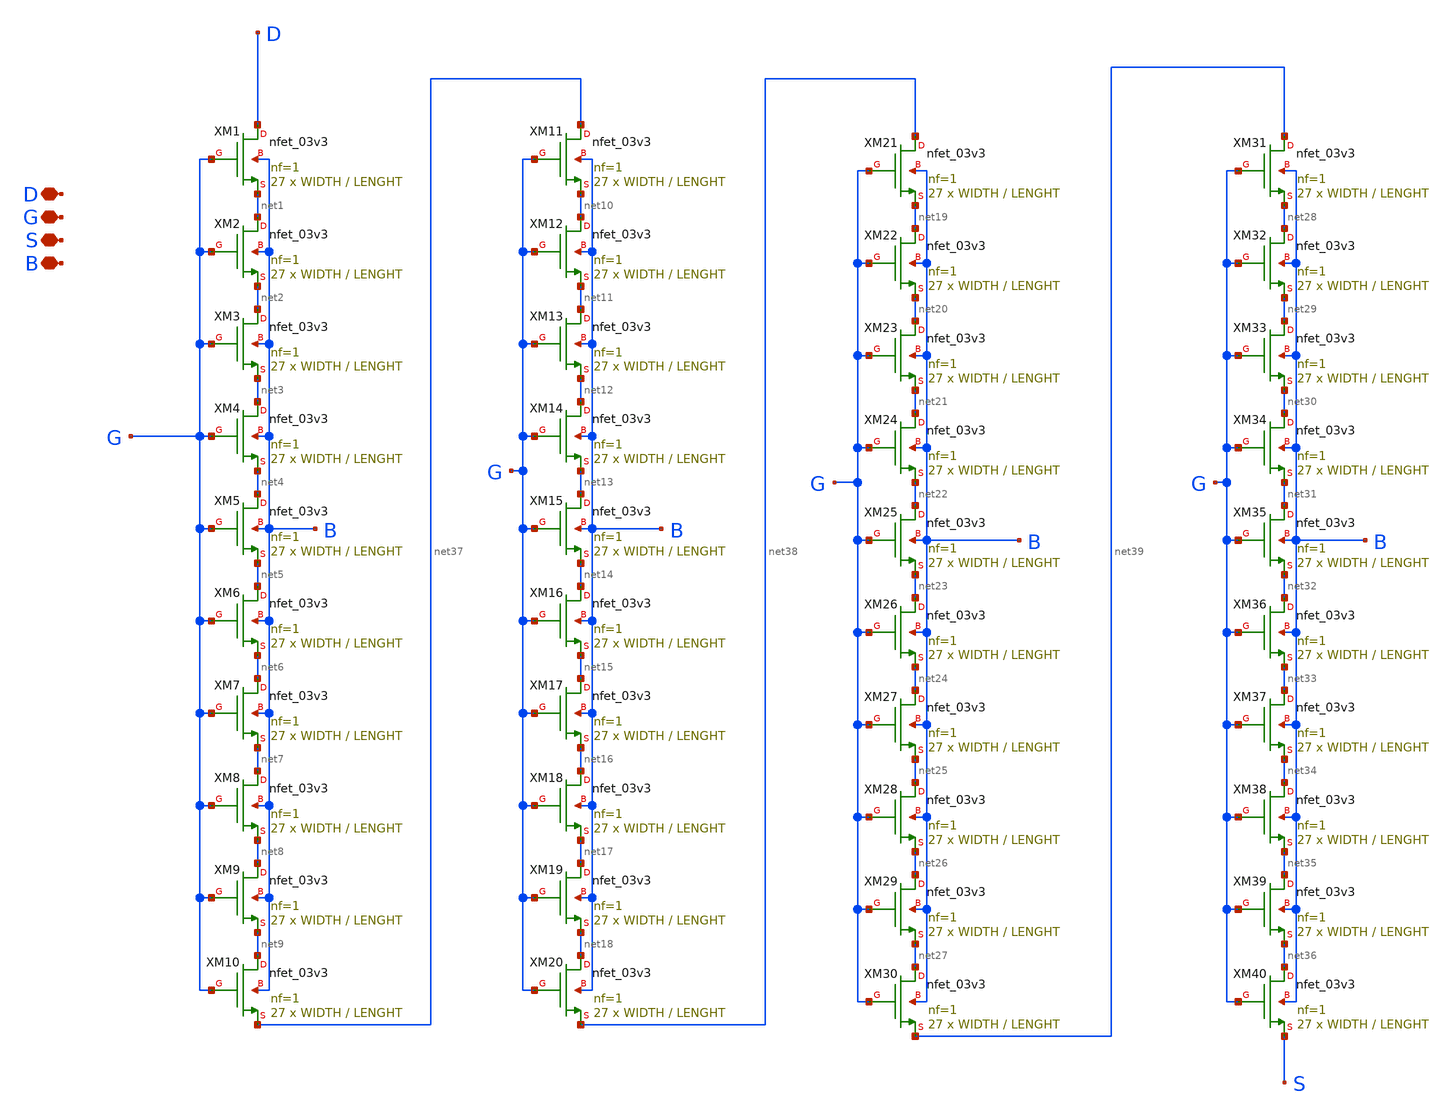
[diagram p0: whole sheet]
** sch_path: New_Extraction/Association/M5_ass.sch
**.subckt M5_ass D G S B
*.iopin D
*.iopin G
*.iopin S
*.iopin B
XM1 D G net1 B nfet_03v3 L=LENGHT W=WIDTH nf=1 ad='int((nf+1)/2) * W/nf * 0.18u' as='int((nf+2)/2) * W/nf * 0.18u'
+ pd='2*int((nf+1)/2) * (W/nf + 0.18u)' ps='2*int((nf+2)/2) * (W/nf + 0.18u)' nrd='0.18u / W' nrs='0.18u / W'
+ sa=0 sb=0 sd=0 m=27
XM2 net1 G net2 B nfet_03v3 L=LENGHT W=WIDTH nf=1 ad='int((nf+1)/2) * W/nf * 0.18u' as='int((nf+2)/2) * W/nf * 0.18u'
+ pd='2*int((nf+1)/2) * (W/nf + 0.18u)' ps='2*int((nf+2)/2) * (W/nf + 0.18u)' nrd='0.18u / W' nrs='0.18u / W'
+ sa=0 sb=0 sd=0 m=27
XM3 net2 G net3 B nfet_03v3 L=LENGHT W=WIDTH nf=1 ad='int((nf+1)/2) * W/nf * 0.18u' as='int((nf+2)/2) * W/nf * 0.18u'
+ pd='2*int((nf+1)/2) * (W/nf + 0.18u)' ps='2*int((nf+2)/2) * (W/nf + 0.18u)' nrd='0.18u / W' nrs='0.18u / W'
+ sa=0 sb=0 sd=0 m=27
XM4 net3 G net4 B nfet_03v3 L=LENGHT W=WIDTH nf=1 ad='int((nf+1)/2) * W/nf * 0.18u' as='int((nf+2)/2) * W/nf * 0.18u'
+ pd='2*int((nf+1)/2) * (W/nf + 0.18u)' ps='2*int((nf+2)/2) * (W/nf + 0.18u)' nrd='0.18u / W' nrs='0.18u / W'
+ sa=0 sb=0 sd=0 m=27
XM5 net4 G net5 B nfet_03v3 L=LENGHT W=WIDTH nf=1 ad='int((nf+1)/2) * W/nf * 0.18u' as='int((nf+2)/2) * W/nf * 0.18u'
+ pd='2*int((nf+1)/2) * (W/nf + 0.18u)' ps='2*int((nf+2)/2) * (W/nf + 0.18u)' nrd='0.18u / W' nrs='0.18u / W'
+ sa=0 sb=0 sd=0 m=27
XM6 net5 G net6 B nfet_03v3 L=LENGHT W=WIDTH nf=1 ad='int((nf+1)/2) * W/nf * 0.18u' as='int((nf+2)/2) * W/nf * 0.18u'
+ pd='2*int((nf+1)/2) * (W/nf + 0.18u)' ps='2*int((nf+2)/2) * (W/nf + 0.18u)' nrd='0.18u / W' nrs='0.18u / W'
+ sa=0 sb=0 sd=0 m=27
XM7 net6 G net7 B nfet_03v3 L=LENGHT W=WIDTH nf=1 ad='int((nf+1)/2) * W/nf * 0.18u' as='int((nf+2)/2) * W/nf * 0.18u'
+ pd='2*int((nf+1)/2) * (W/nf + 0.18u)' ps='2*int((nf+2)/2) * (W/nf + 0.18u)' nrd='0.18u / W' nrs='0.18u / W'
+ sa=0 sb=0 sd=0 m=27
XM8 net7 G net8 B nfet_03v3 L=LENGHT W=WIDTH nf=1 ad='int((nf+1)/2) * W/nf * 0.18u' as='int((nf+2)/2) * W/nf * 0.18u'
+ pd='2*int((nf+1)/2) * (W/nf + 0.18u)' ps='2*int((nf+2)/2) * (W/nf + 0.18u)' nrd='0.18u / W' nrs='0.18u / W'
+ sa=0 sb=0 sd=0 m=27
XM9 net8 G net9 B nfet_03v3 L=LENGHT W=WIDTH nf=1 ad='int((nf+1)/2) * W/nf * 0.18u' as='int((nf+2)/2) * W/nf * 0.18u'
+ pd='2*int((nf+1)/2) * (W/nf + 0.18u)' ps='2*int((nf+2)/2) * (W/nf + 0.18u)' nrd='0.18u / W' nrs='0.18u / W'
+ sa=0 sb=0 sd=0 m=27
XM10 net9 G net37 B nfet_03v3 L=LENGHT W=WIDTH nf=1 ad='int((nf+1)/2) * W/nf * 0.18u' as='int((nf+2)/2) * W/nf * 0.18u'
+ pd='2*int((nf+1)/2) * (W/nf + 0.18u)' ps='2*int((nf+2)/2) * (W/nf + 0.18u)' nrd='0.18u / W' nrs='0.18u / W'
+ sa=0 sb=0 sd=0 m=27
XM11 net37 G net10 B nfet_03v3 L=LENGHT W=WIDTH nf=1 ad='int((nf+1)/2) * W/nf * 0.18u' as='int((nf+2)/2) * W/nf * 0.18u'
+ pd='2*int((nf+1)/2) * (W/nf + 0.18u)' ps='2*int((nf+2)/2) * (W/nf + 0.18u)' nrd='0.18u / W' nrs='0.18u / W'
+ sa=0 sb=0 sd=0 m=27
XM12 net10 G net11 B nfet_03v3 L=LENGHT W=WIDTH nf=1 ad='int((nf+1)/2) * W/nf * 0.18u' as='int((nf+2)/2) * W/nf * 0.18u'
+ pd='2*int((nf+1)/2) * (W/nf + 0.18u)' ps='2*int((nf+2)/2) * (W/nf + 0.18u)' nrd='0.18u / W' nrs='0.18u / W'
+ sa=0 sb=0 sd=0 m=27
XM13 net11 G net12 B nfet_03v3 L=LENGHT W=WIDTH nf=1 ad='int((nf+1)/2) * W/nf * 0.18u' as='int((nf+2)/2) * W/nf * 0.18u'
+ pd='2*int((nf+1)/2) * (W/nf + 0.18u)' ps='2*int((nf+2)/2) * (W/nf + 0.18u)' nrd='0.18u / W' nrs='0.18u / W'
+ sa=0 sb=0 sd=0 m=27
XM14 net12 G net13 B nfet_03v3 L=LENGHT W=WIDTH nf=1 ad='int((nf+1)/2) * W/nf * 0.18u' as='int((nf+2)/2) * W/nf * 0.18u'
+ pd='2*int((nf+1)/2) * (W/nf + 0.18u)' ps='2*int((nf+2)/2) * (W/nf + 0.18u)' nrd='0.18u / W' nrs='0.18u / W'
+ sa=0 sb=0 sd=0 m=27
XM15 net13 G net14 B nfet_03v3 L=LENGHT W=WIDTH nf=1 ad='int((nf+1)/2) * W/nf * 0.18u' as='int((nf+2)/2) * W/nf * 0.18u'
+ pd='2*int((nf+1)/2) * (W/nf + 0.18u)' ps='2*int((nf+2)/2) * (W/nf + 0.18u)' nrd='0.18u / W' nrs='0.18u / W'
+ sa=0 sb=0 sd=0 m=27
XM16 net14 G net15 B nfet_03v3 L=LENGHT W=WIDTH nf=1 ad='int((nf+1)/2) * W/nf * 0.18u' as='int((nf+2)/2) * W/nf * 0.18u'
+ pd='2*int((nf+1)/2) * (W/nf + 0.18u)' ps='2*int((nf+2)/2) * (W/nf + 0.18u)' nrd='0.18u / W' nrs='0.18u / W'
+ sa=0 sb=0 sd=0 m=27
XM17 net15 G net16 B nfet_03v3 L=LENGHT W=WIDTH nf=1 ad='int((nf+1)/2) * W/nf * 0.18u' as='int((nf+2)/2) * W/nf * 0.18u'
+ pd='2*int((nf+1)/2) * (W/nf + 0.18u)' ps='2*int((nf+2)/2) * (W/nf + 0.18u)' nrd='0.18u / W' nrs='0.18u / W'
+ sa=0 sb=0 sd=0 m=27
XM18 net16 G net17 B nfet_03v3 L=LENGHT W=WIDTH nf=1 ad='int((nf+1)/2) * W/nf * 0.18u' as='int((nf+2)/2) * W/nf * 0.18u'
+ pd='2*int((nf+1)/2) * (W/nf + 0.18u)' ps='2*int((nf+2)/2) * (W/nf + 0.18u)' nrd='0.18u / W' nrs='0.18u / W'
+ sa=0 sb=0 sd=0 m=27
XM19 net17 G net18 B nfet_03v3 L=LENGHT W=WIDTH nf=1 ad='int((nf+1)/2) * W/nf * 0.18u' as='int((nf+2)/2) * W/nf * 0.18u'
+ pd='2*int((nf+1)/2) * (W/nf + 0.18u)' ps='2*int((nf+2)/2) * (W/nf + 0.18u)' nrd='0.18u / W' nrs='0.18u / W'
+ sa=0 sb=0 sd=0 m=27
XM20 net18 G net38 B nfet_03v3 L=LENGHT W=WIDTH nf=1 ad='int((nf+1)/2) * W/nf * 0.18u' as='int((nf+2)/2) * W/nf * 0.18u'
+ pd='2*int((nf+1)/2) * (W/nf + 0.18u)' ps='2*int((nf+2)/2) * (W/nf + 0.18u)' nrd='0.18u / W' nrs='0.18u / W'
+ sa=0 sb=0 sd=0 m=27
XM21 net38 G net19 B nfet_03v3 L=LENGHT W=WIDTH nf=1 ad='int((nf+1)/2) * W/nf * 0.18u' as='int((nf+2)/2) * W/nf * 0.18u'
+ pd='2*int((nf+1)/2) * (W/nf + 0.18u)' ps='2*int((nf+2)/2) * (W/nf + 0.18u)' nrd='0.18u / W' nrs='0.18u / W'
+ sa=0 sb=0 sd=0 m=27
XM22 net19 G net20 B nfet_03v3 L=LENGHT W=WIDTH nf=1 ad='int((nf+1)/2) * W/nf * 0.18u' as='int((nf+2)/2) * W/nf * 0.18u'
+ pd='2*int((nf+1)/2) * (W/nf + 0.18u)' ps='2*int((nf+2)/2) * (W/nf + 0.18u)' nrd='0.18u / W' nrs='0.18u / W'
+ sa=0 sb=0 sd=0 m=27
XM23 net20 G net21 B nfet_03v3 L=LENGHT W=WIDTH nf=1 ad='int((nf+1)/2) * W/nf * 0.18u' as='int((nf+2)/2) * W/nf * 0.18u'
+ pd='2*int((nf+1)/2) * (W/nf + 0.18u)' ps='2*int((nf+2)/2) * (W/nf + 0.18u)' nrd='0.18u / W' nrs='0.18u / W'
+ sa=0 sb=0 sd=0 m=27
XM24 net21 G net22 B nfet_03v3 L=LENGHT W=WIDTH nf=1 ad='int((nf+1)/2) * W/nf * 0.18u' as='int((nf+2)/2) * W/nf * 0.18u'
+ pd='2*int((nf+1)/2) * (W/nf + 0.18u)' ps='2*int((nf+2)/2) * (W/nf + 0.18u)' nrd='0.18u / W' nrs='0.18u / W'
+ sa=0 sb=0 sd=0 m=27
XM25 net22 G net23 B nfet_03v3 L=LENGHT W=WIDTH nf=1 ad='int((nf+1)/2) * W/nf * 0.18u' as='int((nf+2)/2) * W/nf * 0.18u'
+ pd='2*int((nf+1)/2) * (W/nf + 0.18u)' ps='2*int((nf+2)/2) * (W/nf + 0.18u)' nrd='0.18u / W' nrs='0.18u / W'
+ sa=0 sb=0 sd=0 m=27
XM26 net23 G net24 B nfet_03v3 L=LENGHT W=WIDTH nf=1 ad='int((nf+1)/2) * W/nf * 0.18u' as='int((nf+2)/2) * W/nf * 0.18u'
+ pd='2*int((nf+1)/2) * (W/nf + 0.18u)' ps='2*int((nf+2)/2) * (W/nf + 0.18u)' nrd='0.18u / W' nrs='0.18u / W'
+ sa=0 sb=0 sd=0 m=27
XM27 net24 G net25 B nfet_03v3 L=LENGHT W=WIDTH nf=1 ad='int((nf+1)/2) * W/nf * 0.18u' as='int((nf+2)/2) * W/nf * 0.18u'
+ pd='2*int((nf+1)/2) * (W/nf + 0.18u)' ps='2*int((nf+2)/2) * (W/nf + 0.18u)' nrd='0.18u / W' nrs='0.18u / W'
+ sa=0 sb=0 sd=0 m=27
XM28 net25 G net26 B nfet_03v3 L=LENGHT W=WIDTH nf=1 ad='int((nf+1)/2) * W/nf * 0.18u' as='int((nf+2)/2) * W/nf * 0.18u'
+ pd='2*int((nf+1)/2) * (W/nf + 0.18u)' ps='2*int((nf+2)/2) * (W/nf + 0.18u)' nrd='0.18u / W' nrs='0.18u / W'
+ sa=0 sb=0 sd=0 m=27
XM29 net26 G net27 B nfet_03v3 L=LENGHT W=WIDTH nf=1 ad='int((nf+1)/2) * W/nf * 0.18u' as='int((nf+2)/2) * W/nf * 0.18u'
+ pd='2*int((nf+1)/2) * (W/nf + 0.18u)' ps='2*int((nf+2)/2) * (W/nf + 0.18u)' nrd='0.18u / W' nrs='0.18u / W'
+ sa=0 sb=0 sd=0 m=27
XM30 net27 G net39 B nfet_03v3 L=LENGHT W=WIDTH nf=1 ad='int((nf+1)/2) * W/nf * 0.18u' as='int((nf+2)/2) * W/nf * 0.18u'
+ pd='2*int((nf+1)/2) * (W/nf + 0.18u)' ps='2*int((nf+2)/2) * (W/nf + 0.18u)' nrd='0.18u / W' nrs='0.18u / W'
+ sa=0 sb=0 sd=0 m=27
XM31 net39 G net28 B nfet_03v3 L=LENGHT W=WIDTH nf=1 ad='int((nf+1)/2) * W/nf * 0.18u' as='int((nf+2)/2) * W/nf * 0.18u'
+ pd='2*int((nf+1)/2) * (W/nf + 0.18u)' ps='2*int((nf+2)/2) * (W/nf + 0.18u)' nrd='0.18u / W' nrs='0.18u / W'
+ sa=0 sb=0 sd=0 m=27
XM32 net28 G net29 B nfet_03v3 L=LENGHT W=WIDTH nf=1 ad='int((nf+1)/2) * W/nf * 0.18u' as='int((nf+2)/2) * W/nf * 0.18u'
+ pd='2*int((nf+1)/2) * (W/nf + 0.18u)' ps='2*int((nf+2)/2) * (W/nf + 0.18u)' nrd='0.18u / W' nrs='0.18u / W'
+ sa=0 sb=0 sd=0 m=27
XM33 net29 G net30 B nfet_03v3 L=LENGHT W=WIDTH nf=1 ad='int((nf+1)/2) * W/nf * 0.18u' as='int((nf+2)/2) * W/nf * 0.18u'
+ pd='2*int((nf+1)/2) * (W/nf + 0.18u)' ps='2*int((nf+2)/2) * (W/nf + 0.18u)' nrd='0.18u / W' nrs='0.18u / W'
+ sa=0 sb=0 sd=0 m=27
XM34 net30 G net31 B nfet_03v3 L=LENGHT W=WIDTH nf=1 ad='int((nf+1)/2) * W/nf * 0.18u' as='int((nf+2)/2) * W/nf * 0.18u'
+ pd='2*int((nf+1)/2) * (W/nf + 0.18u)' ps='2*int((nf+2)/2) * (W/nf + 0.18u)' nrd='0.18u / W' nrs='0.18u / W'
+ sa=0 sb=0 sd=0 m=27
XM35 net31 G net32 B nfet_03v3 L=LENGHT W=WIDTH nf=1 ad='int((nf+1)/2) * W/nf * 0.18u' as='int((nf+2)/2) * W/nf * 0.18u'
+ pd='2*int((nf+1)/2) * (W/nf + 0.18u)' ps='2*int((nf+2)/2) * (W/nf + 0.18u)' nrd='0.18u / W' nrs='0.18u / W'
+ sa=0 sb=0 sd=0 m=27
XM36 net32 G net33 B nfet_03v3 L=LENGHT W=WIDTH nf=1 ad='int((nf+1)/2) * W/nf * 0.18u' as='int((nf+2)/2) * W/nf * 0.18u'
+ pd='2*int((nf+1)/2) * (W/nf + 0.18u)' ps='2*int((nf+2)/2) * (W/nf + 0.18u)' nrd='0.18u / W' nrs='0.18u / W'
+ sa=0 sb=0 sd=0 m=27
XM37 net33 G net34 B nfet_03v3 L=LENGHT W=WIDTH nf=1 ad='int((nf+1)/2) * W/nf * 0.18u' as='int((nf+2)/2) * W/nf * 0.18u'
+ pd='2*int((nf+1)/2) * (W/nf + 0.18u)' ps='2*int((nf+2)/2) * (W/nf + 0.18u)' nrd='0.18u / W' nrs='0.18u / W'
+ sa=0 sb=0 sd=0 m=27
XM38 net34 G net35 B nfet_03v3 L=LENGHT W=WIDTH nf=1 ad='int((nf+1)/2) * W/nf * 0.18u' as='int((nf+2)/2) * W/nf * 0.18u'
+ pd='2*int((nf+1)/2) * (W/nf + 0.18u)' ps='2*int((nf+2)/2) * (W/nf + 0.18u)' nrd='0.18u / W' nrs='0.18u / W'
+ sa=0 sb=0 sd=0 m=27
XM39 net35 G net36 B nfet_03v3 L=LENGHT W=WIDTH nf=1 ad='int((nf+1)/2) * W/nf * 0.18u' as='int((nf+2)/2) * W/nf * 0.18u'
+ pd='2*int((nf+1)/2) * (W/nf + 0.18u)' ps='2*int((nf+2)/2) * (W/nf + 0.18u)' nrd='0.18u / W' nrs='0.18u / W'
+ sa=0 sb=0 sd=0 m=27
XM40 net36 G S B nfet_03v3 L=LENGHT W=WIDTH nf=1 ad='int((nf+1)/2) * W/nf * 0.18u' as='int((nf+2)/2) * W/nf * 0.18u'
+ pd='2*int((nf+1)/2) * (W/nf + 0.18u)' ps='2*int((nf+2)/2) * (W/nf + 0.18u)' nrd='0.18u / W' nrs='0.18u / W'
+ sa=0 sb=0 sd=0 m=27
**.ends
.end
